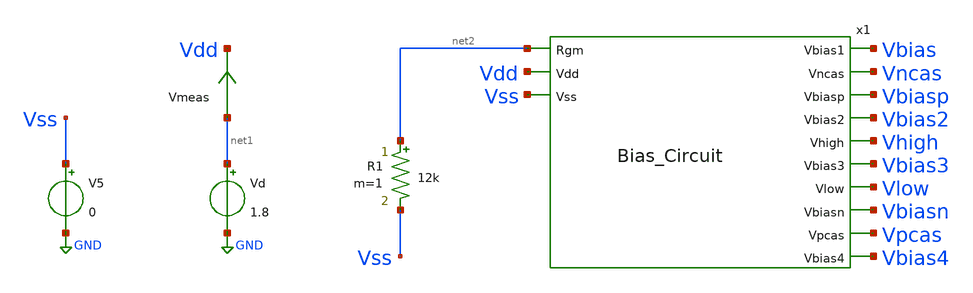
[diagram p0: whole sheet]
** sch_path: src/Opamp_Design/testbenches/Bias_Circuit_tb.sch
**.subckt Bias_Circuit_tb
Vd net1 GND 1.8
Vmeas net1 Vdd 0
.save i(vmeas)
V5 Vss GND 0
R1 net2 Vss 12k m=1
x1 Vbias net2 Vncas Vdd Vbiasp Vbias2 Vhigh Vbias3 Vlow Vbiasn Vss Vpcas Vbias4 Bias_Circuit
**** begin user architecture code

** opencircuitdesign pdks install
.lib $::SKYWATER_MODELS/sky130.lib.spice tt


**** end user architecture code
**.ends

* expanding   symbol:  /foss/designs/FYP/Sky130_Design/Opamp_Design/src/Bias_Circuit.sym # of
*+ pins=13
** sym_path: src/Opamp_Design/src/Bias_Circuit.sym
** sch_path: src/Opamp_Design/src/Bias_Circuit.sch
.subckt Bias_Circuit Vbias1 Rgm Vncas Vdd Vbiasp Vbias2 Vhigh Vbias3 Vlow Vbiasn Vss Vpcas Vbias4
*.ipin Vdd
*.opin Vbiasp
*.ipin Vss
*.opin Vbiasn
*.opin Vbias1
*.opin Vbias2
*.opin Vbias3
*.opin Vbias4
*.opin Vpcas
*.opin Vlow
*.opin Vncas
*.opin Vhigh
*.ipin Rgm
XM1 Vbias3 Vbiasp Vdd Vdd sky130_fd_pr__pfet_01v8_lvt L=1 W=10 nf=1 ad='int((nf+1)/2) * W/nf * 0.29'
+ as='int((nf+2)/2) * W/nf * 0.29' pd='2*int((nf+1)/2) * (W/nf + 0.29)' ps='2*int((nf+2)/2) * (W/nf + 0.29)'
+ nrd='0.29 / W' nrs='0.29 / W' sa=0 sb=0 sd=0 mult=1 m=1
XM2 Vbias3 Vbias3 Vss Vss sky130_fd_pr__nfet_01v8_lvt L=5 W=1.3 nf=1 ad='int((nf+1)/2) * W/nf * 0.29'
+ as='int((nf+2)/2) * W/nf * 0.29' pd='2*int((nf+1)/2) * (W/nf + 0.29)' ps='2*int((nf+2)/2) * (W/nf + 0.29)'
+ nrd='0.29 / W' nrs='0.29 / W' sa=0 sb=0 sd=0 mult=1 m=1
XM3 Vbias4 Vbias3 Vlow Vss sky130_fd_pr__nfet_01v8_lvt L=1 W=5 nf=1 ad='int((nf+1)/2) * W/nf * 0.29'
+ as='int((nf+2)/2) * W/nf * 0.29' pd='2*int((nf+1)/2) * (W/nf + 0.29)' ps='2*int((nf+2)/2) * (W/nf + 0.29)'
+ nrd='0.29 / W' nrs='0.29 / W' sa=0 sb=0 sd=0 mult=1 m=1
XM4 Vlow Vbias4 Vss Vss sky130_fd_pr__nfet_01v8_lvt L=1 W=5 nf=1 ad='int((nf+1)/2) * W/nf * 0.29' as='int((nf+2)/2) * W/nf * 0.29'
+ pd='2*int((nf+1)/2) * (W/nf + 0.29)' ps='2*int((nf+2)/2) * (W/nf + 0.29)' nrd='0.29 / W' nrs='0.29 / W'
+ sa=0 sb=0 sd=0 mult=1 m=1
XM5 Vbias4 Vbiasp Vdd Vdd sky130_fd_pr__pfet_01v8_lvt L=1 W=10 nf=1 ad='int((nf+1)/2) * W/nf * 0.29'
+ as='int((nf+2)/2) * W/nf * 0.29' pd='2*int((nf+1)/2) * (W/nf + 0.29)' ps='2*int((nf+2)/2) * (W/nf + 0.29)'
+ nrd='0.29 / W' nrs='0.29 / W' sa=0 sb=0 sd=0 mult=1 m=1
XM6 net2 net3 Vdd Vdd sky130_fd_pr__pfet_01v8_lvt L=1 W=10 nf=1 ad='int((nf+1)/2) * W/nf * 0.29' as='int((nf+2)/2) * W/nf * 0.29'
+ pd='2*int((nf+1)/2) * (W/nf + 0.29)' ps='2*int((nf+2)/2) * (W/nf + 0.29)' nrd='0.29 / W' nrs='0.29 / W'
+ sa=0 sb=0 sd=0 mult=1 m=1
XM7 net3 Vbias2 net2 Vdd sky130_fd_pr__pfet_01v8_lvt L=1 W=10 nf=1 ad='int((nf+1)/2) * W/nf * 0.29' as='int((nf+2)/2) * W/nf * 0.29'
+ pd='2*int((nf+1)/2) * (W/nf + 0.29)' ps='2*int((nf+2)/2) * (W/nf + 0.29)' nrd='0.29 / W' nrs='0.29 / W'
+ sa=0 sb=0 sd=0 mult=1 m=1
XM8 Vpcas Vpcas net3 Vdd sky130_fd_pr__pfet_01v8_lvt L=1 W=10 nf=1 ad='int((nf+1)/2) * W/nf * 0.29' as='int((nf+2)/2) * W/nf * 0.29'
+ pd='2*int((nf+1)/2) * (W/nf + 0.29)' ps='2*int((nf+2)/2) * (W/nf + 0.29)' nrd='0.29 / W' nrs='0.29 / W'
+ sa=0 sb=0 sd=0 mult=1 m=1
XM9 Vpcas Vbias3 net1 Vss sky130_fd_pr__nfet_01v8_lvt L=1 W=5 nf=1 ad='int((nf+1)/2) * W/nf * 0.29' as='int((nf+2)/2) * W/nf * 0.29'
+ pd='2*int((nf+1)/2) * (W/nf + 0.29)' ps='2*int((nf+2)/2) * (W/nf + 0.29)' nrd='0.29 / W' nrs='0.29 / W'
+ sa=0 sb=0 sd=0 mult=1 m=1
XM10 net1 Vbias4 Vss Vss sky130_fd_pr__nfet_01v8_lvt L=1 W=5 nf=1 ad='int((nf+1)/2) * W/nf * 0.29' as='int((nf+2)/2) * W/nf * 0.29'
+ pd='2*int((nf+1)/2) * (W/nf + 0.29)' ps='2*int((nf+2)/2) * (W/nf + 0.29)' nrd='0.29 / W' nrs='0.29 / W'
+ sa=0 sb=0 sd=0 mult=1 m=1
XM11 Vbias2 Vbias2 Vdd Vdd sky130_fd_pr__pfet_01v8_lvt L=5 W=2 nf=1 ad='int((nf+1)/2) * W/nf * 0.29'
+ as='int((nf+2)/2) * W/nf * 0.29' pd='2*int((nf+1)/2) * (W/nf + 0.29)' ps='2*int((nf+2)/2) * (W/nf + 0.29)'
+ nrd='0.29 / W' nrs='0.29 / W' sa=0 sb=0 sd=0 mult=1 m=1
XM12 Vbias2 Vbias3 net4 Vss sky130_fd_pr__nfet_01v8_lvt L=1 W=5 nf=1 ad='int((nf+1)/2) * W/nf * 0.29'
+ as='int((nf+2)/2) * W/nf * 0.29' pd='2*int((nf+1)/2) * (W/nf + 0.29)' ps='2*int((nf+2)/2) * (W/nf + 0.29)'
+ nrd='0.29 / W' nrs='0.29 / W' sa=0 sb=0 sd=0 mult=1 m=1
XM13 net4 Vbias4 Vss Vss sky130_fd_pr__nfet_01v8_lvt L=1 W=5 nf=1 ad='int((nf+1)/2) * W/nf * 0.29' as='int((nf+2)/2) * W/nf * 0.29'
+ pd='2*int((nf+1)/2) * (W/nf + 0.29)' ps='2*int((nf+2)/2) * (W/nf + 0.29)' nrd='0.29 / W' nrs='0.29 / W'
+ sa=0 sb=0 sd=0 mult=1 m=1
XM14 Vbias1 Vbias3 net5 Vss sky130_fd_pr__nfet_01v8_lvt L=1 W=5 nf=1 ad='int((nf+1)/2) * W/nf * 0.29'
+ as='int((nf+2)/2) * W/nf * 0.29' pd='2*int((nf+1)/2) * (W/nf + 0.29)' ps='2*int((nf+2)/2) * (W/nf + 0.29)'
+ nrd='0.29 / W' nrs='0.29 / W' sa=0 sb=0 sd=0 mult=1 m=1
XM15 net5 Vbias4 Vss Vss sky130_fd_pr__nfet_01v8_lvt L=1 W=5 nf=1 ad='int((nf+1)/2) * W/nf * 0.29' as='int((nf+2)/2) * W/nf * 0.29'
+ pd='2*int((nf+1)/2) * (W/nf + 0.29)' ps='2*int((nf+2)/2) * (W/nf + 0.29)' nrd='0.29 / W' nrs='0.29 / W'
+ sa=0 sb=0 sd=0 mult=1 m=1
XM16 Vbias1 Vbias2 Vhigh Vdd sky130_fd_pr__pfet_01v8_lvt L=1 W=10 nf=1 ad='int((nf+1)/2) * W/nf * 0.29'
+ as='int((nf+2)/2) * W/nf * 0.29' pd='2*int((nf+1)/2) * (W/nf + 0.29)' ps='2*int((nf+2)/2) * (W/nf + 0.29)'
+ nrd='0.29 / W' nrs='0.29 / W' sa=0 sb=0 sd=0 mult=1 m=1
XM17 Vhigh Vbias1 Vdd Vdd sky130_fd_pr__pfet_01v8_lvt L=1 W=10 nf=1 ad='int((nf+1)/2) * W/nf * 0.29'
+ as='int((nf+2)/2) * W/nf * 0.29' pd='2*int((nf+1)/2) * (W/nf + 0.29)' ps='2*int((nf+2)/2) * (W/nf + 0.29)'
+ nrd='0.29 / W' nrs='0.29 / W' sa=0 sb=0 sd=0 mult=1 m=1
XM18 net6 Vbias1 Vdd Vdd sky130_fd_pr__pfet_01v8_lvt L=1 W=10 nf=1 ad='int((nf+1)/2) * W/nf * 0.29' as='int((nf+2)/2) * W/nf * 0.29'
+ pd='2*int((nf+1)/2) * (W/nf + 0.29)' ps='2*int((nf+2)/2) * (W/nf + 0.29)' nrd='0.29 / W' nrs='0.29 / W'
+ sa=0 sb=0 sd=0 mult=1 m=1
XM19 Vncas Vbias2 net6 Vdd sky130_fd_pr__pfet_01v8_lvt L=1 W=10 nf=1 ad='int((nf+1)/2) * W/nf * 0.29'
+ as='int((nf+2)/2) * W/nf * 0.29' pd='2*int((nf+1)/2) * (W/nf + 0.29)' ps='2*int((nf+2)/2) * (W/nf + 0.29)'
+ nrd='0.29 / W' nrs='0.29 / W' sa=0 sb=0 sd=0 mult=1 m=1
XM20 Vncas Vncas net7 Vss sky130_fd_pr__nfet_01v8_lvt L=1 W=5 nf=1 ad='int((nf+1)/2) * W/nf * 0.29' as='int((nf+2)/2) * W/nf * 0.29'
+ pd='2*int((nf+1)/2) * (W/nf + 0.29)' ps='2*int((nf+2)/2) * (W/nf + 0.29)' nrd='0.29 / W' nrs='0.29 / W'
+ sa=0 sb=0 sd=0 mult=1 m=1
XM21 net7 Vbias3 net8 Vss sky130_fd_pr__nfet_01v8_lvt L=1 W=5 nf=1 ad='int((nf+1)/2) * W/nf * 0.29' as='int((nf+2)/2) * W/nf * 0.29'
+ pd='2*int((nf+1)/2) * (W/nf + 0.29)' ps='2*int((nf+2)/2) * (W/nf + 0.29)' nrd='0.29 / W' nrs='0.29 / W'
+ sa=0 sb=0 sd=0 mult=1 m=1
XM22 net8 net7 Vss Vss sky130_fd_pr__nfet_01v8_lvt L=1 W=5 nf=1 ad='int((nf+1)/2) * W/nf * 0.29' as='int((nf+2)/2) * W/nf * 0.29'
+ pd='2*int((nf+1)/2) * (W/nf + 0.29)' ps='2*int((nf+2)/2) * (W/nf + 0.29)' nrd='0.29 / W' nrs='0.29 / W'
+ sa=0 sb=0 sd=0 mult=1 m=1
x1 Rgm Vdd Vss Vbiasp Vbiasn Beta_Multiplier
.ends


* expanding   symbol:  /foss/designs/FYP/Sky130_Design/Opamp_Design/src/Beta_Multiplier.sym # of
*+ pins=5
** sym_path: src/Opamp_Design/src/Beta_Multiplier.sym
** sch_path: src/Opamp_Design/src/Beta_Multiplier.sch
.subckt Beta_Multiplier Rgm Vdd Vss PBias NBias
*.ipin Vdd
*.opin PBias
*.ipin Vss
*.opin NBias
*.ipin Rgm
XM1 NBias PBias Vdd Vdd sky130_fd_pr__pfet_01v8_lvt L=1 W=10 nf=1 ad='int((nf+1)/2) * W/nf * 0.29' as='int((nf+2)/2) * W/nf * 0.29'
+ pd='2*int((nf+1)/2) * (W/nf + 0.29)' ps='2*int((nf+2)/2) * (W/nf + 0.29)' nrd='0.29 / W' nrs='0.29 / W'
+ sa=0 sb=0 sd=0 mult=1 m=1
XM2 NBias NBias Vss Vss sky130_fd_pr__nfet_01v8_lvt L=1 W=5 nf=1 ad='int((nf+1)/2) * W/nf * 0.29' as='int((nf+2)/2) * W/nf * 0.29'
+ pd='2*int((nf+1)/2) * (W/nf + 0.29)' ps='2*int((nf+2)/2) * (W/nf + 0.29)' nrd='0.29 / W' nrs='0.29 / W'
+ sa=0 sb=0 sd=0 mult=1 m=1
XM3 net1 PBias Vdd Vdd sky130_fd_pr__pfet_01v8_lvt L=1 W=10 nf=1 ad='int((nf+1)/2) * W/nf * 0.29' as='int((nf+2)/2) * W/nf * 0.29'
+ pd='2*int((nf+1)/2) * (W/nf + 0.29)' ps='2*int((nf+2)/2) * (W/nf + 0.29)' nrd='0.29 / W' nrs='0.29 / W'
+ sa=0 sb=0 sd=0 mult=1 m=1
XM4 net1 net1 Rgm Vss sky130_fd_pr__nfet_01v8_lvt L=1 W=20 nf=1 ad='int((nf+1)/2) * W/nf * 0.29' as='int((nf+2)/2) * W/nf * 0.29'
+ pd='2*int((nf+1)/2) * (W/nf + 0.29)' ps='2*int((nf+2)/2) * (W/nf + 0.29)' nrd='0.29 / W' nrs='0.29 / W'
+ sa=0 sb=0 sd=0 mult=1 m=1
XM5 net2 net1 Vss Vss sky130_fd_pr__nfet_01v8_lvt L=1 W=5 nf=1 ad='int((nf+1)/2) * W/nf * 0.29' as='int((nf+2)/2) * W/nf * 0.29'
+ pd='2*int((nf+1)/2) * (W/nf + 0.29)' ps='2*int((nf+2)/2) * (W/nf + 0.29)' nrd='0.29 / W' nrs='0.29 / W'
+ sa=0 sb=0 sd=0 mult=1 m=1
XM6 PBias NBias Vss Vss sky130_fd_pr__nfet_01v8_lvt L=1 W=5 nf=1 ad='int((nf+1)/2) * W/nf * 0.29' as='int((nf+2)/2) * W/nf * 0.29'
+ pd='2*int((nf+1)/2) * (W/nf + 0.29)' ps='2*int((nf+2)/2) * (W/nf + 0.29)' nrd='0.29 / W' nrs='0.29 / W'
+ sa=0 sb=0 sd=0 mult=1 m=1
XM7 PBias net2 Vdd Vdd sky130_fd_pr__pfet_01v8_lvt L=1 W=10 nf=1 ad='int((nf+1)/2) * W/nf * 0.29' as='int((nf+2)/2) * W/nf * 0.29'
+ pd='2*int((nf+1)/2) * (W/nf + 0.29)' ps='2*int((nf+2)/2) * (W/nf + 0.29)' nrd='0.29 / W' nrs='0.29 / W'
+ sa=0 sb=0 sd=0 mult=1 m=1
XM8 net2 net2 Vdd Vdd sky130_fd_pr__pfet_01v8_lvt L=1 W=10 nf=1 ad='int((nf+1)/2) * W/nf * 0.29' as='int((nf+2)/2) * W/nf * 0.29'
+ pd='2*int((nf+1)/2) * (W/nf + 0.29)' ps='2*int((nf+2)/2) * (W/nf + 0.29)' nrd='0.29 / W' nrs='0.29 / W'
+ sa=0 sb=0 sd=0 mult=1 m=1
XM9 PBias net3 NBias Vss sky130_fd_pr__nfet_01v8_lvt L=1 W=2 nf=1 ad='int((nf+1)/2) * W/nf * 0.29' as='int((nf+2)/2) * W/nf * 0.29'
+ pd='2*int((nf+1)/2) * (W/nf + 0.29)' ps='2*int((nf+2)/2) * (W/nf + 0.29)' nrd='0.29 / W' nrs='0.29 / W'
+ sa=0 sb=0 sd=0 mult=1 m=1
XM10 net3 NBias Vss Vss sky130_fd_pr__nfet_01v8_lvt L=1 W=5 nf=1 ad='int((nf+1)/2) * W/nf * 0.29' as='int((nf+2)/2) * W/nf * 0.29'
+ pd='2*int((nf+1)/2) * (W/nf + 0.29)' ps='2*int((nf+2)/2) * (W/nf + 0.29)' nrd='0.29 / W' nrs='0.29 / W'
+ sa=0 sb=0 sd=0 mult=1 m=1
XM11 net3 net3 Vdd Vdd sky130_fd_pr__pfet_01v8_lvt L=10 W=1 nf=1 ad='int((nf+1)/2) * W/nf * 0.29' as='int((nf+2)/2) * W/nf * 0.29'
+ pd='2*int((nf+1)/2) * (W/nf + 0.29)' ps='2*int((nf+2)/2) * (W/nf + 0.29)' nrd='0.29 / W' nrs='0.29 / W'
+ sa=0 sb=0 sd=0 mult=1 m=1
.ends

.GLOBAL GND
**** begin user architecture code



* ngspice commands
.options savecurrents

.control
save all
save @m.x1.xm5.msky130_fd_pr__pfet_01v8_lvt[gm]
save @m.x1.xm1.msky130_fd_pr__pfet_01v8_lvt[gm]
save @m.x1.xm2.msky130_fd_pr__nfet_01v8_lvt[gm]
save @m.x1.xm3.msky130_fd_pr__nfet_01v8_lvt[gm]
save @m.x1.xm4.msky130_fd_pr__nfet_01v8_lvt[gm]
save @m.x1.xm6.msky130_fd_pr__pfet_01v8_lvt[gm]
save @m.x1.xm7.msky130_fd_pr__pfet_01v8_lvt[gm]
save @m.x1.xm8.msky130_fd_pr__pfet_01v8_lvt[gm]
save @m.x1.xm9.msky130_fd_pr__nfet_01v8_lvt[gm]
save @m.x1.xm10.msky130_fd_pr__nfet_01v8_lvt[gm]
save @m.x1.xm11.msky130_fd_pr__pfet_01v8_lvt[gm]
save @m.x1.xm12.msky130_fd_pr__nfet_01v8_lvt[gm]
save @m.x1.xm13.msky130_fd_pr__nfet_01v8_lvt[gm]
save @m.x1.xm14.msky130_fd_pr__nfet_01v8_lvt[gm]
save @m.x1.xm15.msky130_fd_pr__nfet_01v8_lvt[gm]
save @m.x1.xm16.msky130_fd_pr__pfet_01v8_lvt[gm]
save @m.x1.xm17.msky130_fd_pr__pfet_01v8_lvt[gm]
save @m.x1.xm18.msky130_fd_pr__nfet_01v8_lvt[gm]
save @m.x1.xm19.msky130_fd_pr__nfet_01v8_lvt[gm]
save @m.x1.xm20.msky130_fd_pr__pfet_01v8_lvt[gm]
save @m.x1.xm21.msky130_fd_pr__pfet_01v8_lvt[gm]
save @m.x1.xm22.msky130_fd_pr__nfet_01v8_lvt[gm]

save @m.x1.x1.xm1.msky130_fd_pr__pfet_01v8_lvt[gm]
save @m.x1.x1.xm2.msky130_fd_pr__nfet_01v8_lvt[gm]
save @m.x1.x1.xm3.msky130_fd_pr__pfet_01v8_lvt[gm]
save @m.x1.x1.xm4.msky130_fd_pr__nfet_01v8_lvt[gm]
save @m.x1.x1.xm5.msky130_fd_pr__nfet_01v8_lvt[gm]
save @m.x1.x1.xm6.msky130_fd_pr__nfet_01v8_lvt[gm]
save @m.x1.x1.xm7.msky130_fd_pr__pfet_01v8_lvt[gm]
save @m.x1.x1.xm8.msky130_fd_pr__pfet_01v8_lvt[gm]
save @m.x1.x1.xm9.msky130_fd_pr__nfet_01v8_lvt[gm]
save @m.x1.x1.xm10.msky130_fd_pr__nfet_01v8_lvt[gm]
save @m.x1.x1.xm11.msky130_fd_pr__pfet_01v8_lvt[gm]

save @m.x1.xm5.msky130_fd_pr__pfet_01v8_lvt[vth]
save @m.x1.xm1.msky130_fd_pr__pfet_01v8_lvt[vth]
save @m.x1.xm2.msky130_fd_pr__nfet_01v8_lvt[vth]
save @m.x1.xm3.msky130_fd_pr__nfet_01v8_lvt[vth]
save @m.x1.xm4.msky130_fd_pr__nfet_01v8_lvt[vth]
save @m.x1.xm6.msky130_fd_pr__pfet_01v8_lvt[vth]
save @m.x1.xm7.msky130_fd_pr__pfet_01v8_lvt[vth]
save @m.x1.xm8.msky130_fd_pr__pfet_01v8_lvt[vth]
save @m.x1.xm9.msky130_fd_pr__nfet_01v8_lvt[vth]
save @m.x1.xm10.msky130_fd_pr__nfet_01v8_lvt[vth]
save @m.x1.xm11.msky130_fd_pr__pfet_01v8_lvt[vth]
save @m.x1.xm12.msky130_fd_pr__nfet_01v8_lvt[vth]
save @m.x1.xm13.msky130_fd_pr__nfet_01v8_lvt[vth]
save @m.x1.xm14.msky130_fd_pr__nfet_01v8_lvt[vth]
save @m.x1.xm15.msky130_fd_pr__nfet_01v8_lvt[vth]
save @m.x1.xm16.msky130_fd_pr__pfet_01v8_lvt[vth]
save @m.x1.xm17.msky130_fd_pr__pfet_01v8_lvt[vth]
save @m.x1.xm18.msky130_fd_pr__nfet_01v8_lvt[vth]
save @m.x1.xm19.msky130_fd_pr__nfet_01v8_lvt[vth]
save @m.x1.xm20.msky130_fd_pr__pfet_01v8_lvt[vth]
save @m.x1.xm21.msky130_fd_pr__pfet_01v8_lvt[vth]
save @m.x1.xm22.msky130_fd_pr__nfet_01v8_lvt[vth]

save @m.x1.x1.xm1.msky130_fd_pr__pfet_01v8_lvt[vth]
save @m.x1.x1.xm2.msky130_fd_pr__nfet_01v8_lvt[vth]
save @m.x1.x1.xm3.msky130_fd_pr__pfet_01v8_lvt[vth]
save @m.x1.x1.xm4.msky130_fd_pr__nfet_01v8_lvt[vth]
save @m.x1.x1.xm5.msky130_fd_pr__nfet_01v8_lvt[vth]
save @m.x1.x1.xm6.msky130_fd_pr__nfet_01v8_lvt[vth]
save @m.x1.x1.xm7.msky130_fd_pr__pfet_01v8_lvt[vth]
save @m.x1.x1.xm8.msky130_fd_pr__pfet_01v8_lvt[vth]
save @m.x1.x1.xm9.msky130_fd_pr__nfet_01v8_lvt[vth]
save @m.x1.x1.xm10.msky130_fd_pr__nfet_01v8_lvt[vth]
save @m.x1.x1.xm11.msky130_fd_pr__pfet_01v8_lvt[vth]

op
*dc Vd 0 2 0.1
*plot i(v.x1.vref)
write Bias_circuit.raw
.endc



**** end user architecture code
.end
